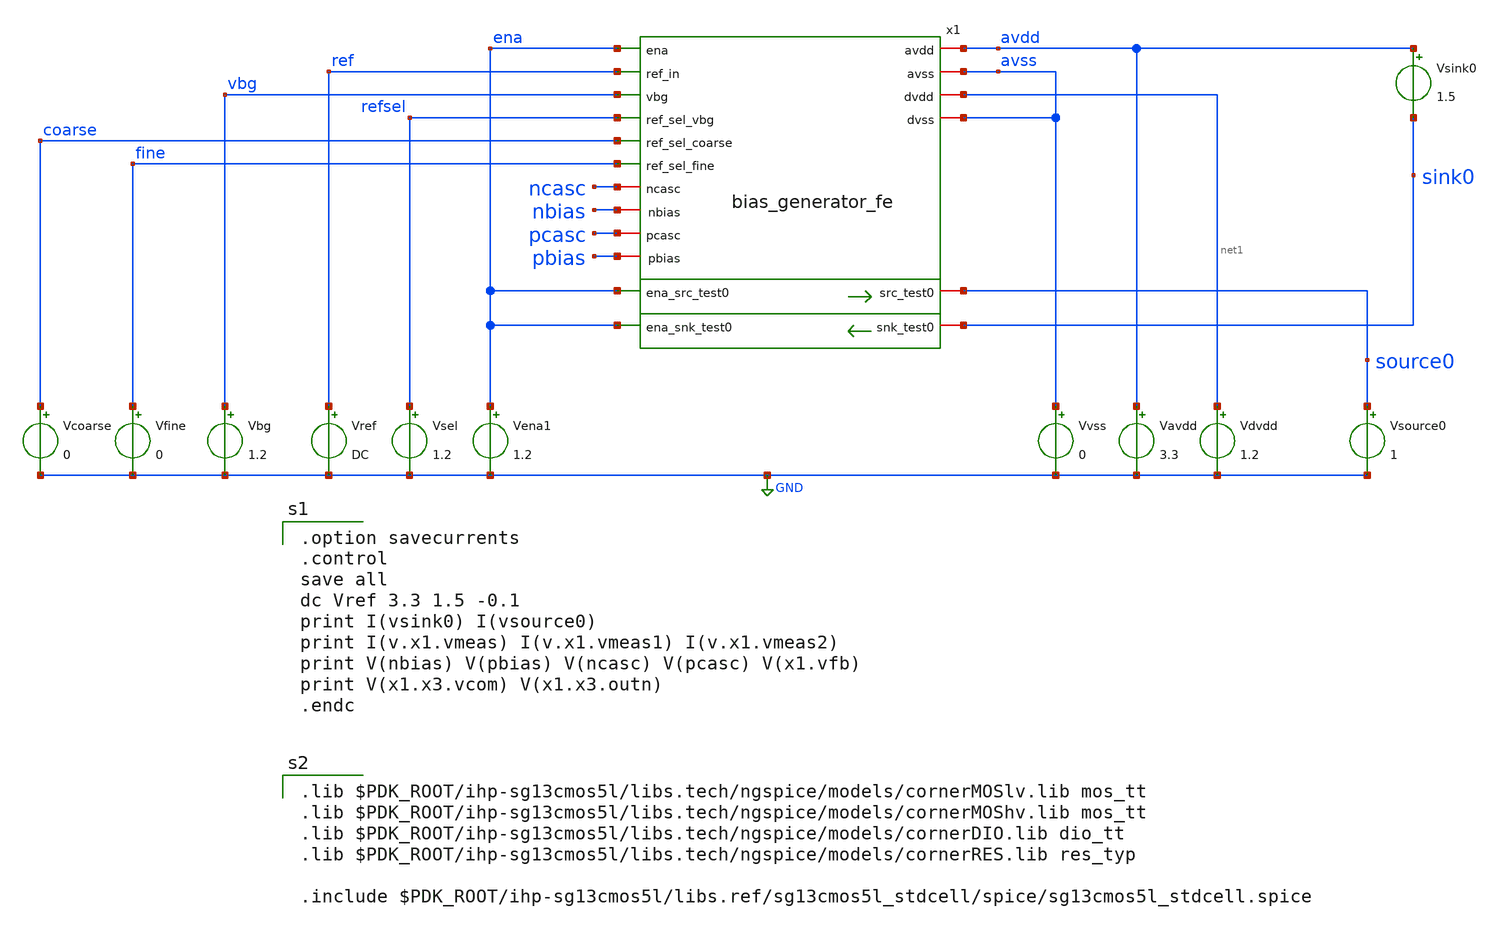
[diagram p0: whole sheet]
** sch_path: xschem/bias_gen_fe_tb.sch
**.subckt bias_gen_fe_tb
Vavdd avdd GND 3.3
Vvss avss GND 0
Vsource0 source0 GND 1
Vsink0 avdd sink0 1.5
Vsel refsel GND 1.2
Vref ref GND DC
Vbg vbg GND 1.2
Vena1 ena GND 1.2
Vdvdd net1 GND 1.2
x1 avdd ena vbg source0 avss net1 ena refsel ref avss nbias pcasc pbias sink0 ena ncasc fine coarse
+ bias_generator_fe
Vfine fine GND 0
Vcoarse coarse GND 0
**** begin user architecture code

.option savecurrents
.control
save all
dc Vref 3.3 1.5 -0.1
print I(vsink0) I(vsource0)
print I(v.x1.vmeas) I(v.x1.vmeas1) I(v.x1.vmeas2)
print V(nbias) V(pbias) V(ncasc) V(pcasc) V(x1.vfb)
print V(x1.x3.vcom) V(x1.x3.outn)
.endc


.lib $PDK_ROOT/ihp-sg13cmos5l/libs.tech/ngspice/models/cornerMOSlv.lib mos_tt
.lib $PDK_ROOT/ihp-sg13cmos5l/libs.tech/ngspice/models/cornerMOShv.lib mos_tt
.lib $PDK_ROOT/ihp-sg13cmos5l/libs.tech/ngspice/models/cornerDIO.lib dio_tt
.lib $PDK_ROOT/ihp-sg13cmos5l/libs.tech/ngspice/models/cornerRES.lib res_typ

.include $PDK_ROOT/ihp-sg13cmos5l/libs.ref/sg13cmos5l_stdcell/spice/sg13cmos5l_stdcell.spice


**** end user architecture code
**.ends
.GLOBAL GND
.end
